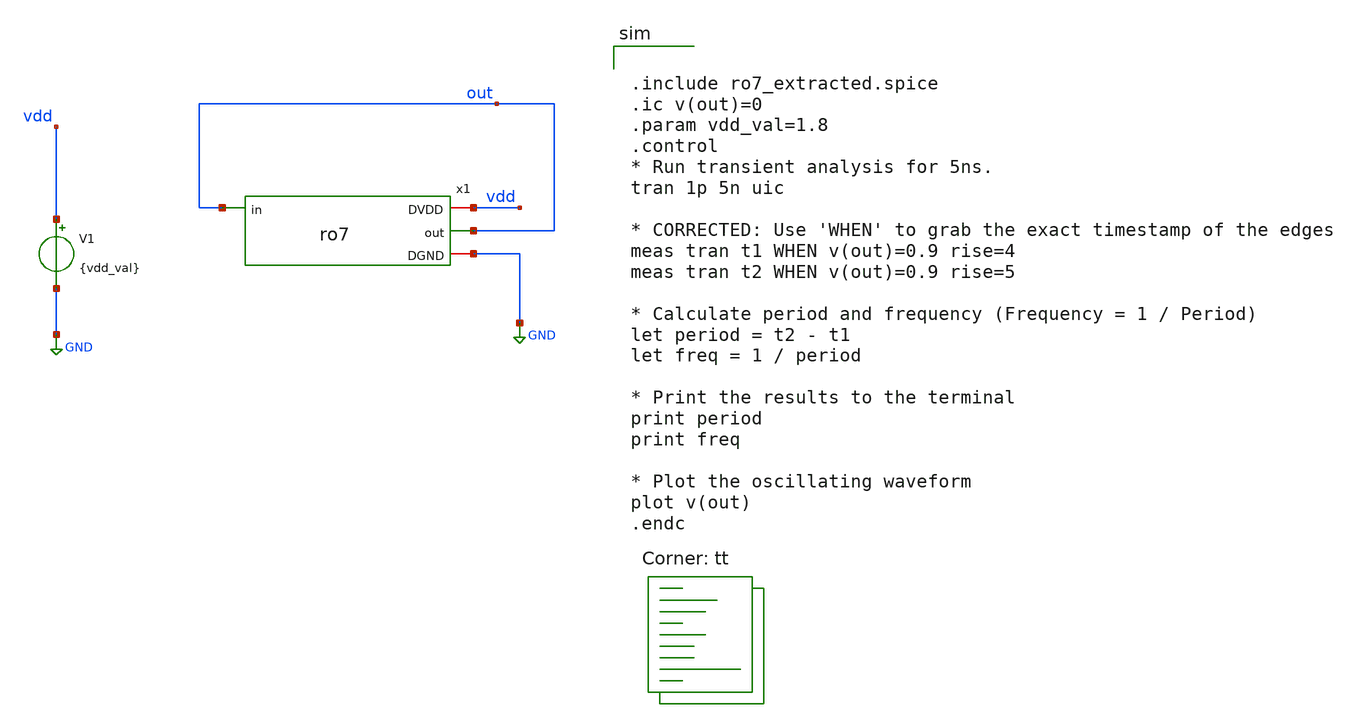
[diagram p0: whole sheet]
** sch_path: assignments/assignment4/ro7_tb.sch
**.subckt ro7_tb
x1 vdd out out GND ro7
V1 vdd GND {vdd_val}
**** begin user architecture code


.include ro7_extracted.spice
.ic v(out)=0
.param vdd_val=1.8
.control
* Run transient analysis for 5ns.
tran 1p 5n uic

* CORRECTED: Use 'WHEN' to grab the exact timestamp of the edges
meas tran t1 WHEN v(out)=0.9 rise=4
meas tran t2 WHEN v(out)=0.9 rise=5

* Calculate period and frequency (Frequency = 1 / Period)
let period = t2 - t1
let freq = 1 / period

* Print the results to the terminal
print period
print freq

* Plot the oscillating waveform
plot v(out)
.endc


.lib $::SKYWATER_MODELS/sky130.lib.spice tt
**** end user architecture code
**.ends

* expanding   symbol:  ro7.sym # of pins=4
** sym_path: assignments/assignment4/ro7.sym
** sch_path: assignments/assignment4/ro7.sch
.subckt ro7 DVDD in out DGND
*.ipin in
*.opin out
*.iopin DVDD
*.iopin DGND
x1 DVDD in net1 DGND inv
x2 DVDD net1 net2 DGND inv
x3 DVDD net2 net3 DGND inv
x4 DVDD net3 net4 DGND inv
x5 DVDD net4 net5 DGND inv
x6 DVDD net5 net6 DGND inv
x7 DVDD net6 out DGND inv
.ends


* expanding   symbol:  inv.sym # of pins=8
** sym_path: assignments/assignment4/inv.sym
** sch_path: assignments/assignment4/inv.sch
.subckt inv DVDD in out DGND
*.ipin in
*.opin out
*.iopin DVDD
*.iopin DGND
XM3 out in DVDD DVDD sky130_fd_pr__pfet_01v8 L=0.15 W=0.84 nf=1 ad='int((nf+1)/2) * W/nf * 0.29' as='int((nf+2)/2) * W/nf * 0.29'
+ pd='2*int((nf+1)/2) * (W/nf + 0.29)' ps='2*int((nf+2)/2) * (W/nf + 0.29)' nrd='0.29 / W' nrs='0.29 / W'
+ sa=0 sb=0 sd=0 mult=1 m=1
XM2 out in DGND DGND sky130_fd_pr__nfet_01v8 L=0.15 W=0.42 nf=1 ad='int((nf+1)/2) * W/nf * 0.29' as='int((nf+2)/2) * W/nf * 0.29'
+ pd='2*int((nf+1)/2) * (W/nf + 0.29)' ps='2*int((nf+2)/2) * (W/nf + 0.29)' nrd='0.29 / W' nrs='0.29 / W'
+ sa=0 sb=0 sd=0 mult=1 m=1
.ends

.GLOBAL GND
.end
